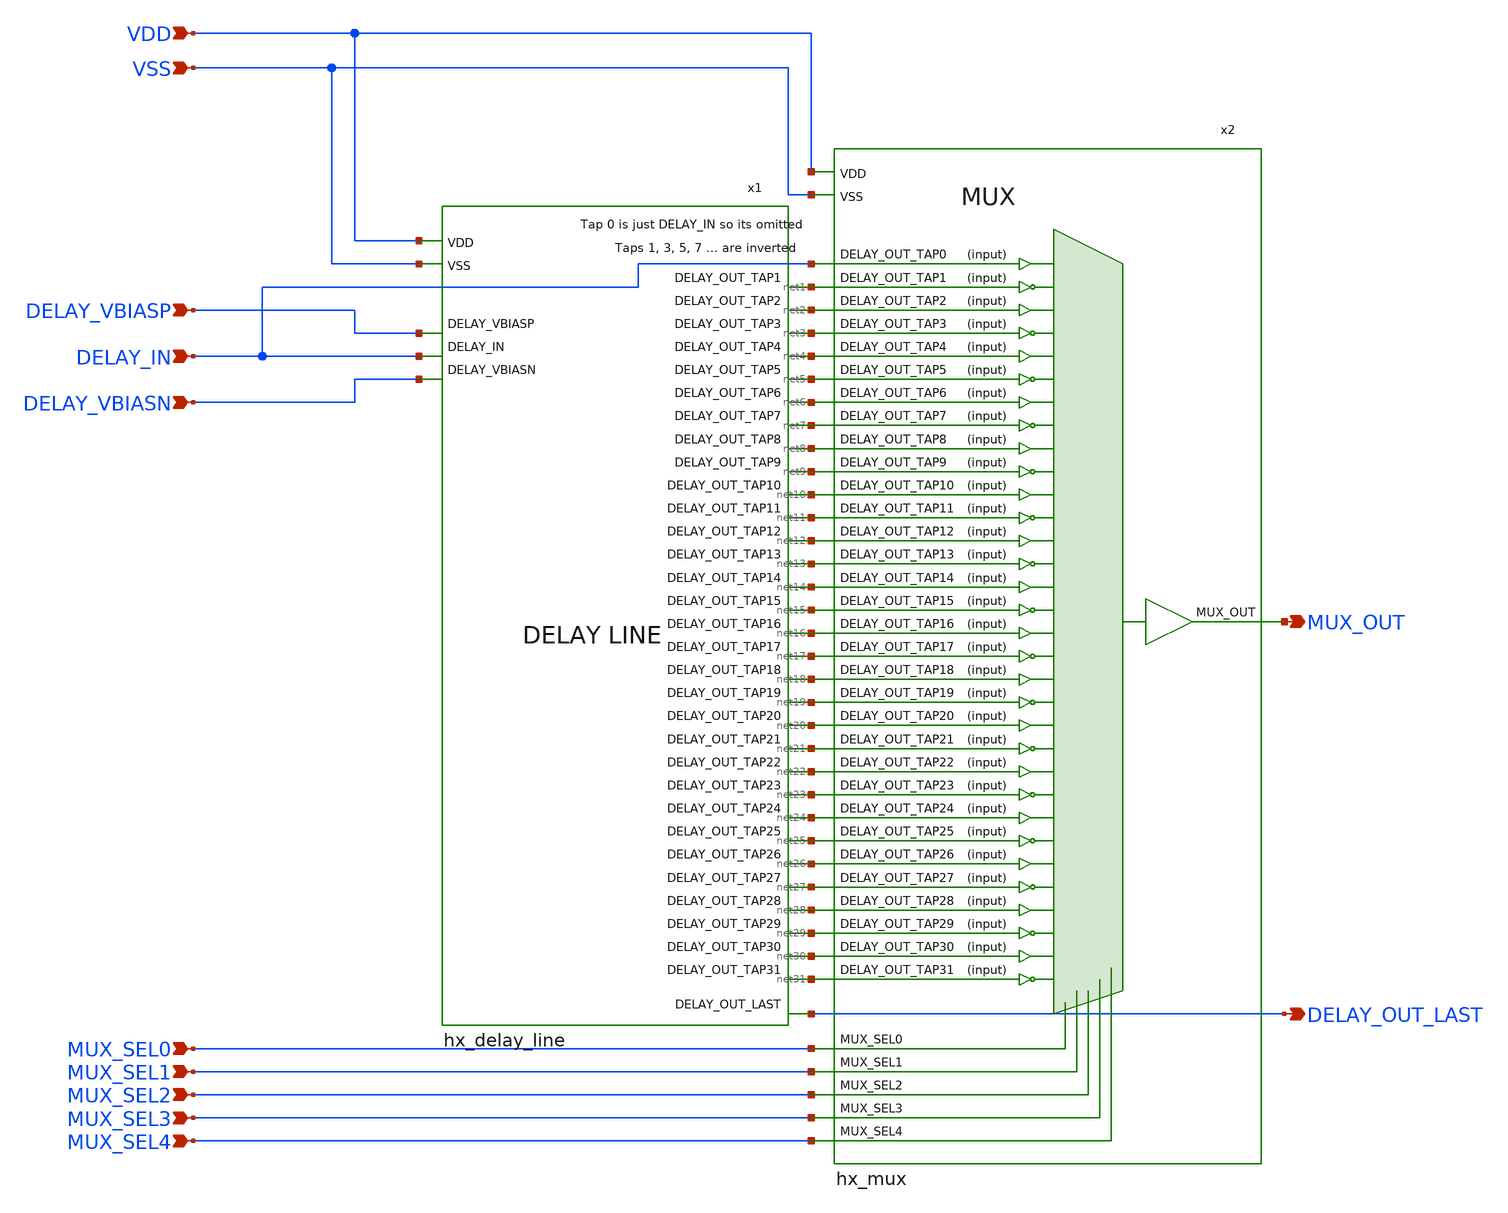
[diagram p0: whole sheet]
** sch_path: schematics/hx_delay_line_with_mux.sch
**.subckt hx_delay_line_with_mux VDD VSS MUX_OUT DELAY_IN DELAY_VBIASP DELAY_VBIASN DELAY_OUT_LAST
*+ MUX_SEL0 MUX_SEL1 MUX_SEL2 MUX_SEL3 MUX_SEL4
*.ipin VDD
*.ipin VSS
*.opin MUX_OUT
*.ipin DELAY_IN
*.ipin DELAY_VBIASP
*.ipin DELAY_VBIASN
*.opin DELAY_OUT_LAST
*.ipin MUX_SEL0
*.ipin MUX_SEL1
*.ipin MUX_SEL2
*.ipin MUX_SEL3
*.ipin MUX_SEL4
x1 VSS VDD DELAY_OUT_LAST net1 net2 net3 net4 net5 net6 net7 net8 net9 net10 net11 net12 net13 net14
+ net15 net16 net17 net18 net19 net20 net21 net22 net23 net24 net25 net26 net27 net28 net29 net30 net31
+ DELAY_IN DELAY_VBIASN DELAY_VBIASP hx_delay_line
x2 VSS VDD DELAY_IN net1 net2 net3 net4 net5 net6 net7 net8 net9 net10 net11 net12 net13 net14 net15
+ net16 net17 net18 net19 net20 net21 net22 net23 net24 net25 net26 net27 net28 net29 net30 net31 MUX_SEL0
+ MUX_SEL1 MUX_OUT MUX_SEL4 MUX_SEL2 MUX_SEL3 hx_mux
**.ends
.end
